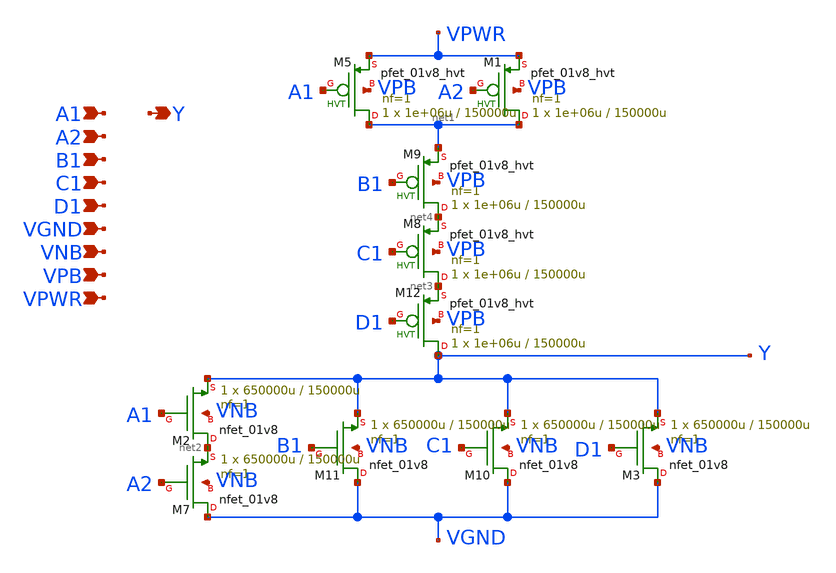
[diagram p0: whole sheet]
** sch_path: schematics/a2111oi/sky130_fd_sc_hd__a2111oi_1.sch
**.subckt sky130_fd_sc_hd__a2111oi_1 A1 A2 B1 C1 D1 VGND VNB VPB VPWR Y
*.ipin A1
*.ipin A2
*.ipin B1
*.ipin C1
*.ipin D1
*.ipin VGND
*.ipin VNB
*.ipin VPB
*.ipin VPWR
*.opin Y
XM1 net1 A2 VPWR VPB sky130_fd_pr__pfet_01v8_hvt L=150000u W=1e+06u nf=1 ad='int((1 + 1)/2) * 1e+06u / 1 * 0.29'
+ as='int((1 + 2)/2) * 1e+06u / 1 * 0.29' pd='2*int((1 + 1)/2) * (1e+06u / 1 + 0.29)' ps='2*int((1 + 2)/2) * (1e+06u / 1 + 0.29)'
+ nrd='0.29 / 1e+06u ' nrs='0.29 / 1e+06u ' sa=0 sb=0 sd=0 mult=1 m=1
XM2 net2 A1 Y VNB sky130_fd_pr__nfet_01v8 L=150000u W=650000u nf=1 ad='int((1 + 1)/2) * 650000u / 1 * 0.29'
+ as='int((1 + 2)/2) * 650000u / 1 * 0.29' pd='2*int((1 + 1)/2) * (650000u / 1 + 0.29)' ps='2*int((1 + 2)/2) * (650000u / 1 + 0.29)'
+ nrd='0.29 / 650000u ' nrs='0.29 / 650000u ' sa=0 sb=0 sd=0 mult=1 m=1
XM3 VGND D1 Y VNB sky130_fd_pr__nfet_01v8 L=150000u W=650000u nf=1 ad='int((1 + 1)/2) * 650000u / 1 * 0.29'
+ as='int((1 + 2)/2) * 650000u / 1 * 0.29' pd='2*int((1 + 1)/2) * (650000u / 1 + 0.29)' ps='2*int((1 + 2)/2) * (650000u / 1 + 0.29)'
+ nrd='0.29 / 650000u ' nrs='0.29 / 650000u ' sa=0 sb=0 sd=0 mult=1 m=1
XM5 net1 A1 VPWR VPB sky130_fd_pr__pfet_01v8_hvt L=150000u W=1e+06u nf=1 ad='int((1 + 1)/2) * 1e+06u / 1 * 0.29'
+ as='int((1 + 2)/2) * 1e+06u / 1 * 0.29' pd='2*int((1 + 1)/2) * (1e+06u / 1 + 0.29)' ps='2*int((1 + 2)/2) * (1e+06u / 1 + 0.29)'
+ nrd='0.29 / 1e+06u ' nrs='0.29 / 1e+06u ' sa=0 sb=0 sd=0 mult=1 m=1
XM8 net3 C1 net4 VPB sky130_fd_pr__pfet_01v8_hvt L=150000u W=1e+06u nf=1 ad='int((1 + 1)/2) * 1e+06u / 1 * 0.29'
+ as='int((1 + 2)/2) * 1e+06u / 1 * 0.29' pd='2*int((1 + 1)/2) * (1e+06u / 1 + 0.29)' ps='2*int((1 + 2)/2) * (1e+06u / 1 + 0.29)'
+ nrd='0.29 / 1e+06u ' nrs='0.29 / 1e+06u ' sa=0 sb=0 sd=0 mult=1 m=1
XM9 net4 B1 net1 VPB sky130_fd_pr__pfet_01v8_hvt L=150000u W=1e+06u nf=1 ad='int((1 + 1)/2) * 1e+06u / 1 * 0.29'
+ as='int((1 + 2)/2) * 1e+06u / 1 * 0.29' pd='2*int((1 + 1)/2) * (1e+06u / 1 + 0.29)' ps='2*int((1 + 2)/2) * (1e+06u / 1 + 0.29)'
+ nrd='0.29 / 1e+06u ' nrs='0.29 / 1e+06u ' sa=0 sb=0 sd=0 mult=1 m=1
XM7 VGND A2 net2 VNB sky130_fd_pr__nfet_01v8 L=150000u W=650000u nf=1 ad='int((1 + 1)/2) * 650000u / 1 * 0.29'
+ as='int((1 + 2)/2) * 650000u / 1 * 0.29' pd='2*int((1 + 1)/2) * (650000u / 1 + 0.29)' ps='2*int((1 + 2)/2) * (650000u / 1 + 0.29)'
+ nrd='0.29 / 650000u ' nrs='0.29 / 650000u ' sa=0 sb=0 sd=0 mult=1 m=1
XM10 VGND C1 Y VNB sky130_fd_pr__nfet_01v8 L=150000u W=650000u nf=1 ad='int((1 + 1)/2) * 650000u / 1 * 0.29'
+ as='int((1 + 2)/2) * 650000u / 1 * 0.29' pd='2*int((1 + 1)/2) * (650000u / 1 + 0.29)' ps='2*int((1 + 2)/2) * (650000u / 1 + 0.29)'
+ nrd='0.29 / 650000u ' nrs='0.29 / 650000u ' sa=0 sb=0 sd=0 mult=1 m=1
XM11 VGND B1 Y VNB sky130_fd_pr__nfet_01v8 L=150000u W=650000u nf=1 ad='int((1 + 1)/2) * 650000u / 1 * 0.29'
+ as='int((1 + 2)/2) * 650000u / 1 * 0.29' pd='2*int((1 + 1)/2) * (650000u / 1 + 0.29)' ps='2*int((1 + 2)/2) * (650000u / 1 + 0.29)'
+ nrd='0.29 / 650000u ' nrs='0.29 / 650000u ' sa=0 sb=0 sd=0 mult=1 m=1
XM12 Y D1 net3 VPB sky130_fd_pr__pfet_01v8_hvt L=150000u W=1e+06u nf=1 ad='int((1 + 1)/2) * 1e+06u / 1 * 0.29'
+ as='int((1 + 2)/2) * 1e+06u / 1 * 0.29' pd='2*int((1 + 1)/2) * (1e+06u / 1 + 0.29)' ps='2*int((1 + 2)/2) * (1e+06u / 1 + 0.29)'
+ nrd='0.29 / 1e+06u ' nrs='0.29 / 1e+06u ' sa=0 sb=0 sd=0 mult=1 m=1
**.ends
.end
